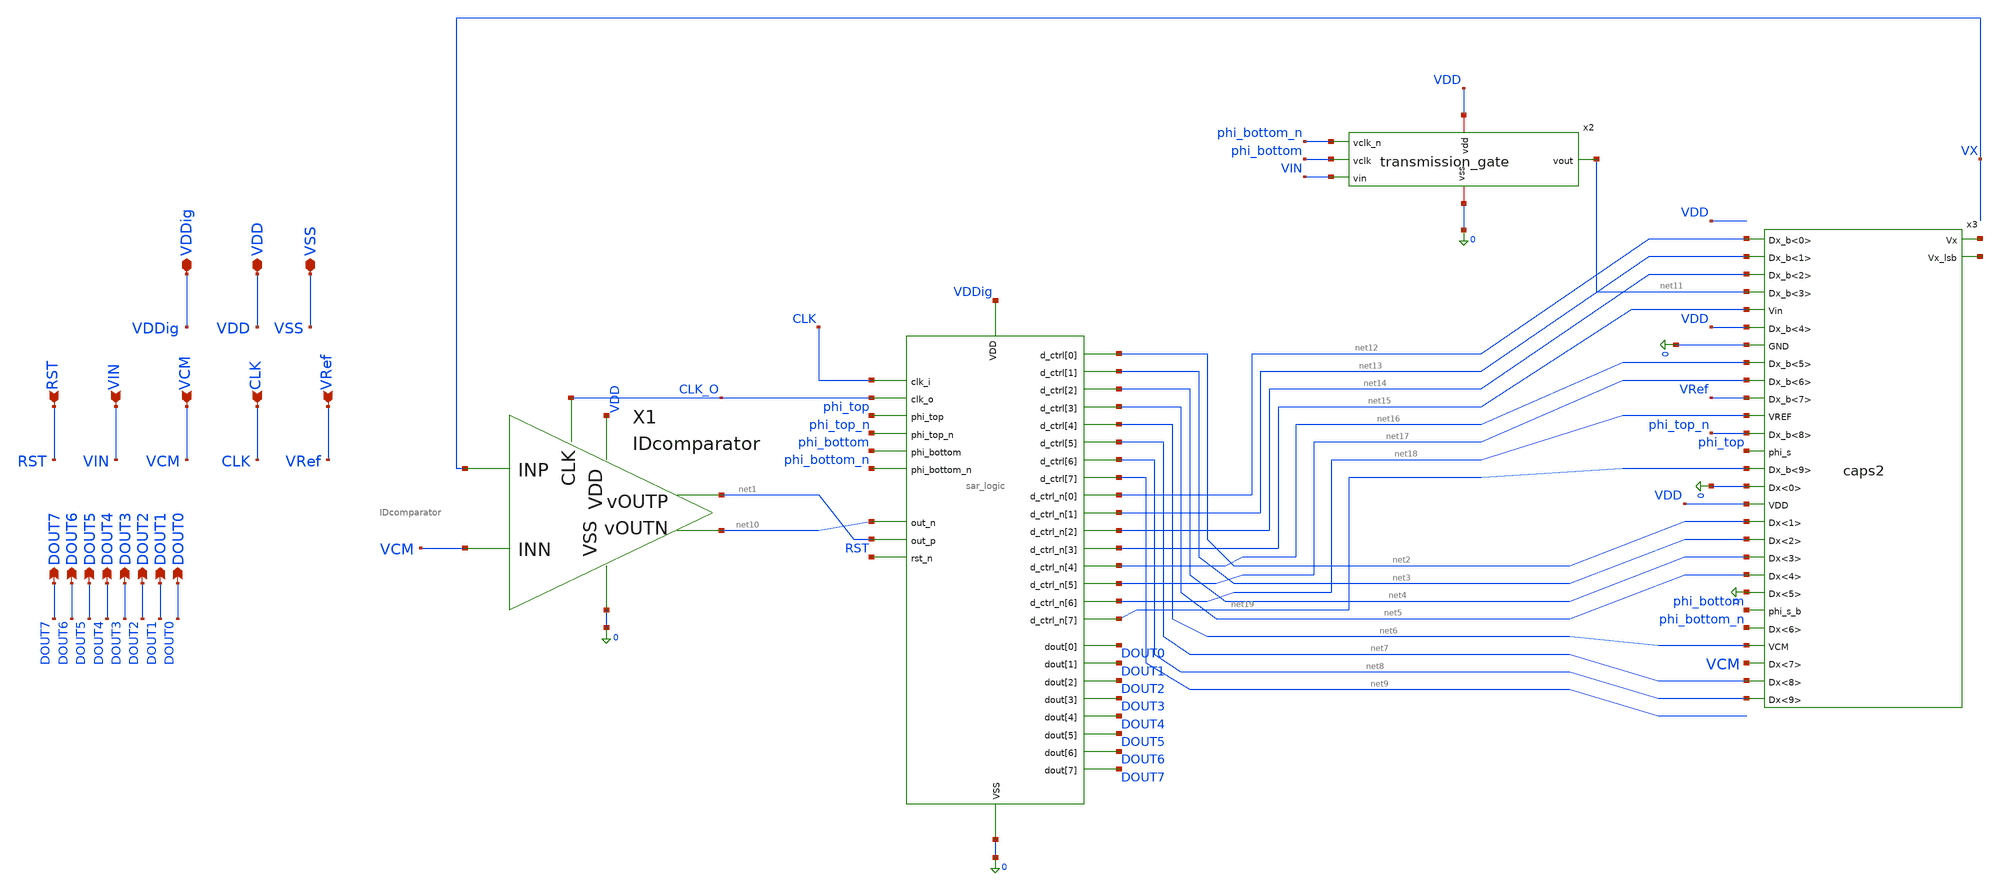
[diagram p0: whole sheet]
** sch_path: analog/top/top.sch
**.subckt top VSS VDD CLK VRef DOUT7 VCM VIN RST DOUT6 DOUT5 DOUT4 DOUT3 DOUT2 DOUT1 DOUT0 VDDig
*.iopin VSS
*.iopin VDD
*.ipin CLK
*.ipin VRef
*.opin DOUT7
*.ipin VCM
*.ipin VIN
*.ipin RST
*.opin DOUT6
*.opin DOUT5
*.opin DOUT4
*.opin DOUT3
*.opin DOUT2
*.opin DOUT1
*.opin DOUT0
*.iopin VDDig
x2 VDD net11 phi_bottom_n phi_bottom VIN 0 transmission_gate
X4 VDDig 0 CLK_O net2 net3 net4 net5 net6 net7 net8 net9 DOUT0 DOUT2 DOUT3 DOUT4 DOUT5 DOUT6 DOUT7
+ net10 net1 RST phi_top phi_top_n phi_bottom phi_bottom_n CLK DOUT1 net12 net13 net14 net15 net16 net17
+ net18 net19 sar_adc_logic
X1 VX VCM CLK_O VDD 0 net1 net10 IDcomparator
x3 net12 net13 net14 net11 net15 VDD 0 net16 net17 VRef net18 phi_top_n phi_top net19 0 VDD net2
+ net20 net3 net4 net21 net5 0 phi_bottom phi_bottom_n net6 VCM net7 net8 caps2
**** begin user architecture code


.include /foss/designs/chipathon-2026-ti-adc/analog/digital/SAR_ADC_LOGIC/sar_adc_logic.spice
.include /foss/designs/chipathon-2026-ti-adc/analog/blocks/IDcomparator/IDcomparator.spice



.include $::180MCU_MODELS/design.ngspice
.include $PDK_ROOT/gf180mcuD/libs.ref/gf180mcu_fd_sc_mcu7t5v0/spice/gf180mcu_fd_sc_mcu7t5v0.spice
.lib $::180MCU_MODELS/sm141064.ngspice typical
.lib $::180MCU_MODELS/smbb000149.ngspice typical
.lib /foss/pdks/gf180mcuD/libs.tech/ngspice/sm141064.ngspice cap_mim
.lib /foss/pdks/gf180mcuD/libs.tech/ngspice/sm141064.ngspice mimcap_typical

**** end user architecture code
**.ends
.end
